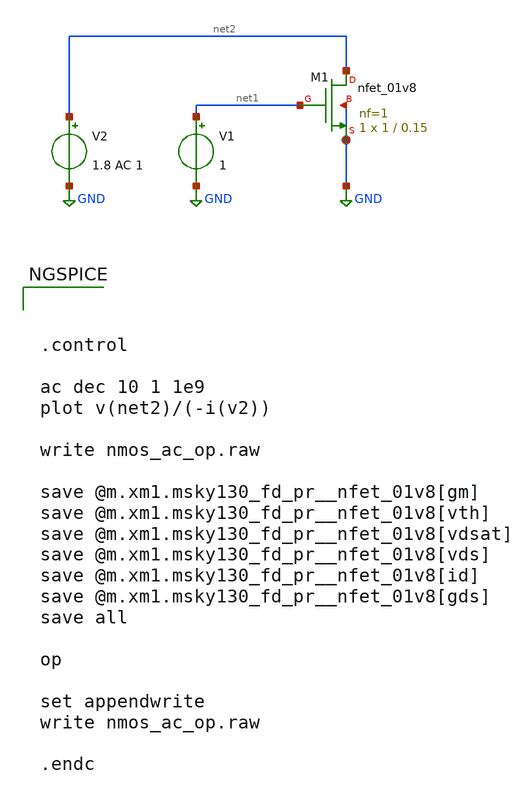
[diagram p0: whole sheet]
** sch_path: examples/xschem/nmos_ac_op.sch
**.subckt nmos_ac_op
XM1 net2 net1 GND GND sky130_fd_pr__nfet_01v8 L=0.15 W=1 nf=1 ad='int((nf+1)/2) * W/nf * 0.29' as='int((nf+2)/2) * W/nf * 0.29'
+ pd='2*int((nf+1)/2) * (W/nf + 0.29)' ps='2*int((nf+2)/2) * (W/nf + 0.29)' nrd='0.29 / W' nrs='0.29 / W'
+ sa=0 sb=0 sd=0 mult=1 m=1
V1 net1 GND 1
V2 net2 GND 1.8 AC 1
**** begin user architecture code



.control

ac dec 10 1 1e9
plot v(net2)/(-i(v2))

write nmos_ac_op.raw

save @m.xm1.msky130_fd_pr__nfet_01v8[gm]
save @m.xm1.msky130_fd_pr__nfet_01v8[vth]
save @m.xm1.msky130_fd_pr__nfet_01v8[vdsat]
save @m.xm1.msky130_fd_pr__nfet_01v8[vds]
save @m.xm1.msky130_fd_pr__nfet_01v8[id]
save @m.xm1.msky130_fd_pr__nfet_01v8[gds]
save all

op

set appendwrite
write nmos_ac_op.raw

.endc



** opencircuitdesign pdks install
.lib $::SKYWATER_MODELS/sky130.lib.spice tt


**** end user architecture code
**.ends
.GLOBAL GND
.end
